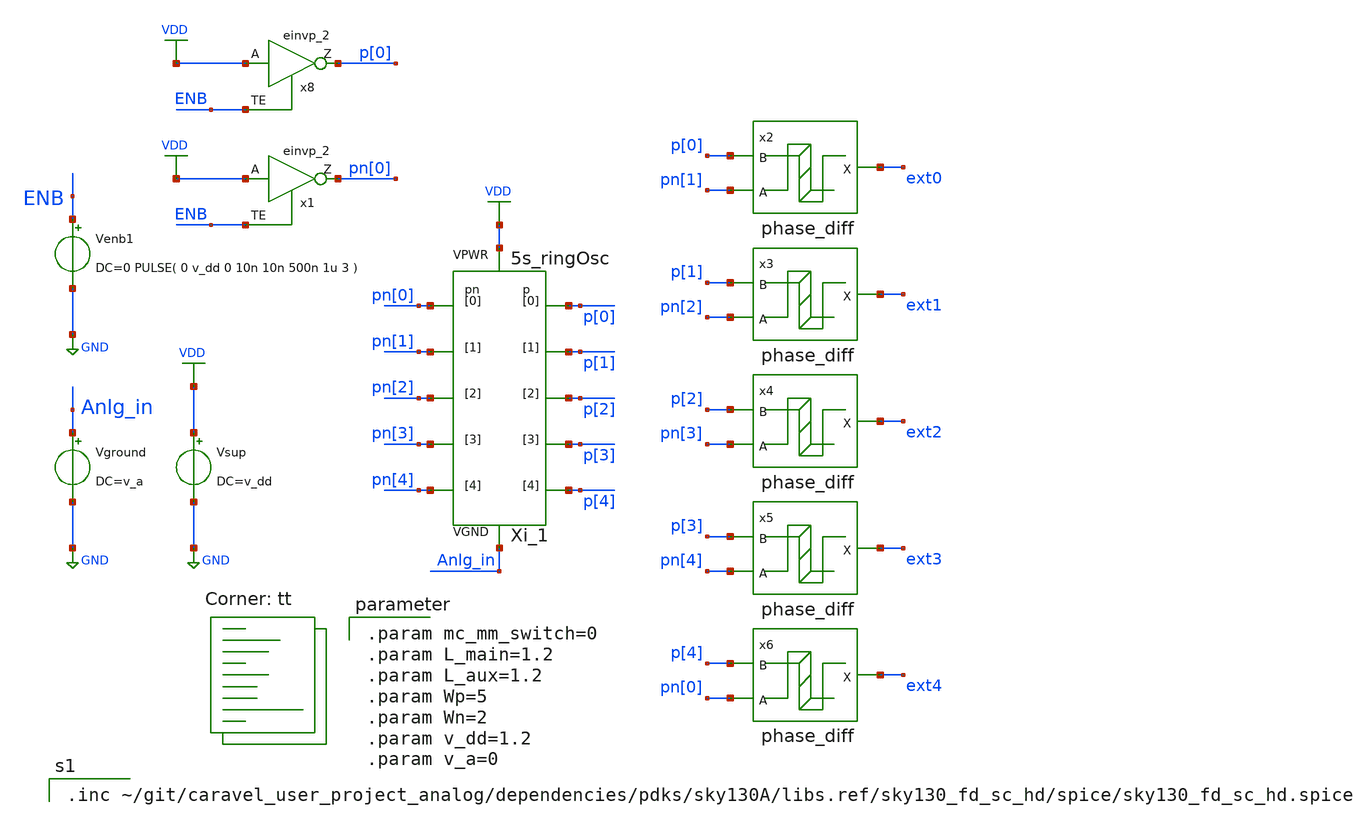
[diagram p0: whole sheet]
** sch_path: xschem/tb/5s_ringOsc_tb.sch
**.subckt 5s_ringOsc_tb
Vsup VDD GND DC=v_dd
Vground Anlg_in GND DC=v_a
Venb1 ENB GND DC=0 PULSE( 0 v_dd 0 10n 10n 500n 1u 3 )
Xi_1 Anlg_in VDD p[0] p[1] p[2] p[3] p[4] pn[0] pn[1] pn[2] pn[3] pn[4] 5s_ringOsc L_main="L_main"
+ L_aux="L_aux" Wp="Wp" Wn="Wn"
x1 VDD ENB GND GND VDD VDD pn[0] sky130_fd_sc_hd__einvp_2
x8 VDD ENB GND GND VDD VDD p[0] sky130_fd_sc_hd__einvp_2
x2 p[0] ext0 pn[1] phase_diff
x3 p[1] ext1 pn[2] phase_diff
x4 p[2] ext2 pn[3] phase_diff
x5 p[3] ext3 pn[4] phase_diff
x6 p[4] ext4 pn[0] phase_diff
**** begin user architecture code


.control
set nobreak
set num_threads=6
set test_mode = 0
* mode = 0: operation testing				1:  frequency extraction    2:  power consumption
if ($test_mode = 0)
    save p[0] p[1] p[2] p[3] p[4]  pn[0] pn[1] pn[2] pn[3] pn[4] enb sink_out d_ext0 d_ext1 d_ext2
+ d_ext3 d_ext4
    TRAN 5n 100u
    plot p[0]
    plot sink_out
    * MEAS TRAN prd TRIG p_buf[0] VAL=0.8 RISE=10 TARG p_buf[0] VAL=0.8 RISE=20
    * let freq = 10/prd
    * echo "frequency: "
    * print freq
    write 5s_ringOsc_tb.raw
    eprvcd sink_out d_ext0 d_ext1 d_ext2 d_ext3 d_ext4
end
if ($test_mode = 1)
    let Vlow = 0
    let Vlimit = 1.01     $ set upper bound for sweeping
    let Vsweep = 0.2      $ set step size for sweeping
    let NoPoints=(Vlimit-Vlow)/Vsweep+2    $ set number of points for sweeping
    let freq =unitvec(NoPoints)
    let Vin  =unitvec(NoPoints)
    let Vin[0]=Vlow
    let ix=0
    while Vin[ix] < Vlimit
        alter Vground DC=Vin[ix]
        TRAN 0.4n 12u
        MEAS TRAN prd TRIG pha_vco VAL=0.8 RISE=10 TARG pha_vco VAL=0.8 RISE =20
        let freq[ix] = 10/prd
        let ix = ix+1
        Let Vin[ix] = Vin[ix-1]+Vsweep
    end
   print Vin freq
end
if ($test_mode = 2)
    save "vdd" @Vsup[i] "p[0]"
    TRAN 0.1n 5u
    MEAS TRAN I_vco AVG @Vsup[i] FROM=3u TO=4u
    MEAS TRAN V_vco AVG vdd FROM=3u TO=4u
    let Power=I_vco*V_vco
    print Power
end
.endc



.param mc_mm_switch=0
.param L_main=1.2
.param L_aux=1.2
.param Wp=5
.param Wn=2
.param v_dd=1.2
.param v_a=0

.lib $::SKYWATER_MODELS/sky130.lib.spice tt

.inc ~/git/caravel_user_project_analog/dependencies/pdks/sky130A/libs.ref/sky130_fd_sc_hd/spice/sky130_fd_sc_hd.spice



x_pe sink_out d_ext0 d_ext1 d_ext2 d_ext3 d_ext4 phase_extractor
.subckt phase_extractor sink_out ext0 ext1 ext2 ext3 ext4

a_ext_or0 [ext2 ext3] net3 or1
a_ext_or1 [ext0 ext1] net4 or1
a_ext_or2 [ext4 GND ] net5 or1
a_ext_or3 [net5 GND ] net6 or1
a_ext_or4 [net4 net3] net7 or1
a_ext_or5 [net7 net6] sink_out or1

.model and1 d_and(rise_delay = 0.5e-9 fall_delay = 0.3e-9 input_load = 0.5e-12)
.model inv1 d_inverter(rise_delay = 0.5e-9 fall_delay = 0.3e-9 input_load = 0.5e-12)
.model or1 d_or(rise_delay = 0.5e-9 fall_delay = 0.3e-9 input_load = 0.5e-12)

.ends

*** adc_bridge blocks ***
aconverter [ext0 ext1 ext2 ext3 ext4] [d_ext0 d_ext1 d_ext2 d_ext3 d_ext4] adc1
.model adc1 adc_bridge (in_low='v_dd/2-5m' in_high='v_dd/2+5m' rise_delay=1.0e-12 fall_delay=1.0e-12)







**** end user architecture code
**.ends

* expanding   symbol:  5s_ringOsc.sym # of pins=12
** sym_path: xschem/lib/5s_ringOsc.sym
** sch_path: xschem/lib/5s_ringOsc.sch
.subckt 5s_ringOsc VGND VPWR p[0] p[1] p[2] p[3] p[4] pn[0] pn[1] pn[2] pn[3] pn[4]  L_main=1
+ L_aux=1 Wp=4 Wn=2
*.iopin VPWR
*.iopin VGND
*.opin pn[1]
*.opin p[1]
*.opin p[2]
*.opin p[3]
*.opin p[4]
*.opin pn[2]
*.opin pn[3]
*.opin pn[4]
*.iopin pn[0]
*.opin p[0]
Xi_1 p[4] pn[4] VPWR VGND p[0] pn[0] cc_inv L_main="L_main" L_aux="L_aux" Wp="Wp" Wn="Wn"
Xi_2 p[0] pn[0] VPWR VGND p[1] pn[1] cc_inv L_main="L_main" L_aux="L_aux" Wp="Wp" Wn="Wn"
Xi_3 p[1] pn[1] VPWR VGND p[2] pn[2] cc_inv L_main="L_main" L_aux="L_aux" Wp="Wp" Wn="Wn"
Xi_4 p[2] pn[2] VPWR VGND p[3] pn[3] cc_inv L_main="L_main" L_aux="L_aux" Wp="Wp" Wn="Wn"
Xi_5 p[3] pn[3] VPWR VGND p[4] pn[4] cc_inv L_main="L_main" L_aux="L_aux" Wp="Wp" Wn="Wn"
.ends


* expanding   symbol:  phase_diff.sym # of pins=3
** sym_path: xschem/lib/phase_diff.sym
** sch_path: xschem/lib/phase_diff.sch
.subckt phase_diff A X B
*.ipin A
*.ipin B
*.opin X
x_ext_and A net1 GND GND VDD VDD X sky130_fd_sc_hd__and2_2
x_ext_inv B GND GND VDD VDD net1 sky130_fd_sc_hd__inv_2
.ends


* expanding   symbol:  cc_inv.sym # of pins=6
** sym_path: xschem/lib/cc_inv.sym
** sch_path: xschem/lib/cc_inv.sch
.subckt cc_inv inp inn VPWR VGND outp outn  L_main=1 L_aux=1 Wp=4 Wn=2
*.opin outp
*.ipin inn
*.iopin VGND
*.opin outn
*.ipin inp
*.iopin VPWR
Xi_1 inp VPWR VGND outp main_inv l="L_main" wp="Wp" wn="Wn"
Xi_2 inn VPWR VGND outn main_inv l="L_main" wp="Wp" wn="Wn"
Xi_3 outp VPWR VGND outn aux_inv L="L_aux" Wp="Wp" Wn="Wn"
Xi_4 outn VPWR VGND outp aux_inv L="L_aux" Wp="Wp" Wn="Wn"
.ends


* expanding   symbol:  main_inv.sym # of pins=4
** sym_path: main_inv.sym
** sch_path: main_inv.sch
.subckt main_inv A VPWR VGND Y  l=0.15 wp=1.2 wn=0.6
*.iopin VPWR
*.iopin VGND
*.ipin A
*.opin Y
XM1 Y A VPWR VDD sky130_fd_pr__pfet_01v8 L="L" W="Wp" nf=1 ad='int((1 + 1)/2) * "Wp" / 1 * 0.29' as='int((1 + 2)/2) * "Wp" / 1 * 0.29'
+ pd='2*int((1 + 1)/2) * ("Wp" / 1 + 0.29)' ps='2*int((1 + 2)/2) * ("Wp" / 1 + 0.29)' nrd='0.29 / "Wp" '
+ nrs='0.29 / "Wp" ' sa=0 sb=0 sd=0 mult=1 m=1
XM2 Y A VGND GND sky130_fd_pr__nfet_01v8 L="L" W="Wn" nf=1 ad='int((nf+1)/2) * W/nf * 0.29' as='int((nf+2)/2) * W/nf * 0.29'
+ pd='2*int((nf+1)/2) * (W/nf + 0.29)' ps='2*int((nf+2)/2) * (W/nf + 0.29)' nrd='0.29 / W' nrs='0.29 / W'
+ sa=0 sb=0 sd=0 mult=1 m=1
XM3 Y A VPWR VDD sky130_fd_pr__pfet_01v8 L="L" W="Wp" nf=1 ad='int((1 + 1)/2) * "Wp" / 1 * 0.29' as='int((1 + 2)/2) * "Wp" / 1 * 0.29'
+ pd='2*int((1 + 1)/2) * ("Wp" / 1 + 0.29)' ps='2*int((1 + 2)/2) * ("Wp" / 1 + 0.29)' nrd='0.29 / "Wp" '
+ nrs='0.29 / "Wp" ' sa=0 sb=0 sd=0 mult=1 m=1
XM4 Y A VGND GND sky130_fd_pr__nfet_01v8 L="L" W="Wn" nf=1 ad='int((nf+1)/2) * W/nf * 0.29' as='int((nf+2)/2) * W/nf * 0.29'
+ pd='2*int((nf+1)/2) * (W/nf + 0.29)' ps='2*int((nf+2)/2) * (W/nf + 0.29)' nrd='0.29 / W' nrs='0.29 / W'
+ sa=0 sb=0 sd=0 mult=1 m=1
XM5 Y A VPWR VDD sky130_fd_pr__pfet_01v8 L="L" W="Wp" nf=1 ad='int((1 + 1)/2) * "Wp" / 1 * 0.29' as='int((1 + 2)/2) * "Wp" / 1 * 0.29'
+ pd='2*int((1 + 1)/2) * ("Wp" / 1 + 0.29)' ps='2*int((1 + 2)/2) * ("Wp" / 1 + 0.29)' nrd='0.29 / "Wp" '
+ nrs='0.29 / "Wp" ' sa=0 sb=0 sd=0 mult=1 m=1
XM6 Y A VGND GND sky130_fd_pr__nfet_01v8 L="L" W="Wn" nf=1 ad='int((nf+1)/2) * W/nf * 0.29' as='int((nf+2)/2) * W/nf * 0.29'
+ pd='2*int((nf+1)/2) * (W/nf + 0.29)' ps='2*int((nf+2)/2) * (W/nf + 0.29)' nrd='0.29 / W' nrs='0.29 / W'
+ sa=0 sb=0 sd=0 mult=1 m=1
XM7 Y A VPWR VDD sky130_fd_pr__pfet_01v8 L="L" W="Wp" nf=1 ad='int((1 + 1)/2) * "Wp" / 1 * 0.29' as='int((1 + 2)/2) * "Wp" / 1 * 0.29'
+ pd='2*int((1 + 1)/2) * ("Wp" / 1 + 0.29)' ps='2*int((1 + 2)/2) * ("Wp" / 1 + 0.29)' nrd='0.29 / "Wp" '
+ nrs='0.29 / "Wp" ' sa=0 sb=0 sd=0 mult=1 m=1
XM8 Y A VGND GND sky130_fd_pr__nfet_01v8 L="L" W="Wn" nf=1 ad='int((nf+1)/2) * W/nf * 0.29' as='int((nf+2)/2) * W/nf * 0.29'
+ pd='2*int((nf+1)/2) * (W/nf + 0.29)' ps='2*int((nf+2)/2) * (W/nf + 0.29)' nrd='0.29 / W' nrs='0.29 / W'
+ sa=0 sb=0 sd=0 mult=1 m=1
.ends


* expanding   symbol:  aux_inv.sym # of pins=4
** sym_path: xschem/lib/aux_inv.sym
** sch_path: xschem/lib/aux_inv.sch
.subckt aux_inv A VPWR VGND Y  L=0.15 Wp=1.2 Wn=0.65
*.iopin VPWR
*.iopin VGND
*.ipin A
*.opin Y
XM1 Y A VPWR VDD sky130_fd_pr__pfet_01v8 L="L" W="Wp" nf=1 ad='int((1 + 1)/2) * "Wp" / 1 * 0.29' as='int((1 + 2)/2) * "Wp" / 1 * 0.29'
+ pd='2*int((1 + 1)/2) * ("Wp" / 1 + 0.29)' ps='2*int((1 + 2)/2) * ("Wp" / 1 + 0.29)' nrd='0.29 / "Wp" '
+ nrs='0.29 / "Wp" ' sa=0 sb=0 sd=0 mult=1 m=1
XM2 Y A VGND GND sky130_fd_pr__nfet_01v8 L="L" W="Wn" nf=1 ad='int((nf+1)/2) * W/nf * 0.29' as='int((nf+2)/2) * W/nf * 0.29'
+ pd='2*int((nf+1)/2) * (W/nf + 0.29)' ps='2*int((nf+2)/2) * (W/nf + 0.29)' nrd='0.29 / W' nrs='0.29 / W'
+ sa=0 sb=0 sd=0 mult=1 m=1
.ends

.GLOBAL VDD
.GLOBAL GND
.end
